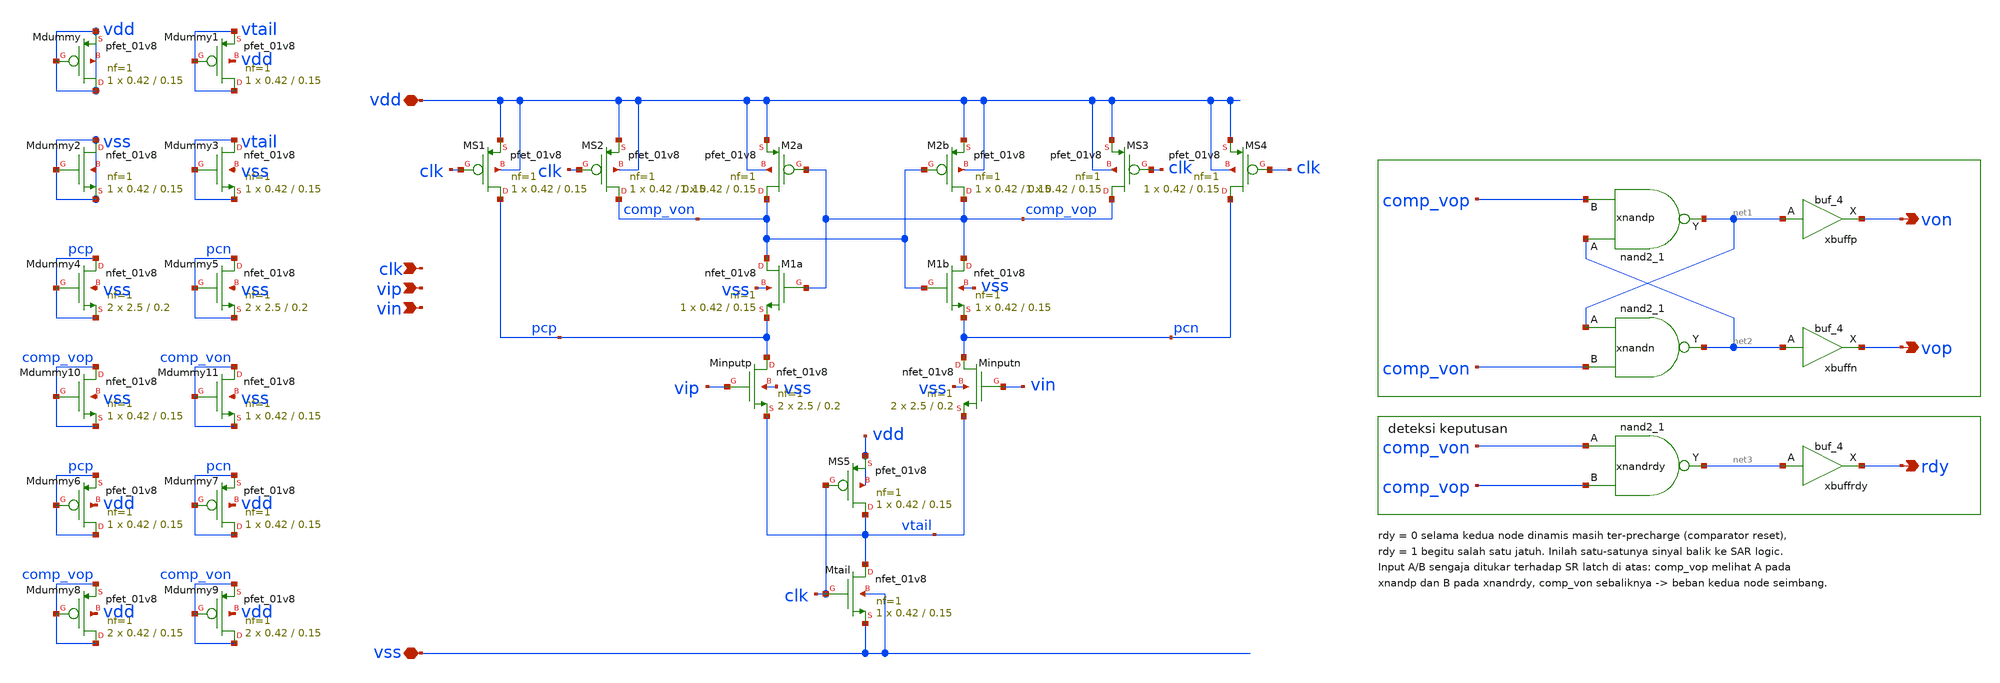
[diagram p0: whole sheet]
** sch_path: xschem/sar-adc/comparator.sch
**.subckt comparator clk vip vin vdd vss vop von rdy
*.ipin clk
*.ipin vip
*.ipin vin
*.iopin vdd
*.iopin vss
*.opin vop
*.opin von
*.opin rdy
XMinputp pcp vip vtail vss sky130_fd_pr__nfet_01v8 L=0.2 W=2.5 nf=1 ad='int((1 + 1)/2) * 2.5 / 1 * 0.29'
+ as='int((1 + 2)/2) * 2.5 / 1 * 0.29' pd='2*int((1 + 1)/2) * (2.5 / 1 + 0.29)' ps='2*int((1 + 2)/2) * (2.5 / 1 + 0.29)'
+ nrd='0.29 / 2.5 ' nrs='0.29 / 2.5 ' sa=0 sb=0 sd=0 mult=2 m=2
XMinputn pcn vin vtail vss sky130_fd_pr__nfet_01v8 L=0.2 W=2.5 nf=1 ad='int((1 + 1)/2) * 2.5 / 1 * 0.29'
+ as='int((1 + 2)/2) * 2.5 / 1 * 0.29' pd='2*int((1 + 1)/2) * (2.5 / 1 + 0.29)' ps='2*int((1 + 2)/2) * (2.5 / 1 + 0.29)'
+ nrd='0.29 / 2.5 ' nrs='0.29 / 2.5 ' sa=0 sb=0 sd=0 mult=2 m=2
XM1a comp_von comp_vop pcp vss sky130_fd_pr__nfet_01v8 L=0.15 W=0.42 nf=1 ad='int((1 + 1)/2) * 0.42 / 1 * 0.29'
+ as='int((1 + 2)/2) * 0.42 / 1 * 0.29' pd='2*int((1 + 1)/2) * (0.42 / 1 + 0.29)' ps='2*int((1 + 2)/2) * (0.42 / 1 + 0.29)'
+ nrd='0.29 / 0.42 ' nrs='0.29 / 0.42 ' sa=0 sb=0 sd=0 mult=1 m=1
XM1b comp_vop comp_von pcn vss sky130_fd_pr__nfet_01v8 L=0.15 W=0.42 nf=1 ad='int((1 + 1)/2) * 0.42 / 1 * 0.29'
+ as='int((1 + 2)/2) * 0.42 / 1 * 0.29' pd='2*int((1 + 1)/2) * (0.42 / 1 + 0.29)' ps='2*int((1 + 2)/2) * (0.42 / 1 + 0.29)'
+ nrd='0.29 / 0.42 ' nrs='0.29 / 0.42 ' sa=0 sb=0 sd=0 mult=1 m=1
XM2a comp_von comp_vop vdd vdd sky130_fd_pr__pfet_01v8 L=0.15 W=0.42 nf=1 ad='int((1 + 1)/2) * 0.42 / 1 * 0.29'
+ as='int((1 + 2)/2) * 0.42 / 1 * 0.29' pd='2*int((1 + 1)/2) * (0.42 / 1 + 0.29)' ps='2*int((1 + 2)/2) * (0.42 / 1 + 0.29)'
+ nrd='0.29 / 0.42 ' nrs='0.29 / 0.42 ' sa=0 sb=0 sd=0 mult=1 m=1
XM2b comp_vop comp_von vdd vdd sky130_fd_pr__pfet_01v8 L=0.15 W=0.42 nf=1 ad='int((1 + 1)/2) * 0.42 / 1 * 0.29'
+ as='int((1 + 2)/2) * 0.42 / 1 * 0.29' pd='2*int((1 + 1)/2) * (0.42 / 1 + 0.29)' ps='2*int((1 + 2)/2) * (0.42 / 1 + 0.29)'
+ nrd='0.29 / 0.42 ' nrs='0.29 / 0.42 ' sa=0 sb=0 sd=0 mult=1 m=1
XMtail vtail clk vss vss sky130_fd_pr__nfet_01v8 L=0.15 W=0.42 nf=1 ad='int((1 + 1)/2) * 0.42 / 1 * 0.29'
+ as='int((1 + 2)/2) * 0.42 / 1 * 0.29' pd='2*int((1 + 1)/2) * (0.42 / 1 + 0.29)' ps='2*int((1 + 2)/2) * (0.42 / 1 + 0.29)'
+ nrd='0.29 / 0.42 ' nrs='0.29 / 0.42 ' sa=0 sb=0 sd=0 mult=1 m=1
XMS3 comp_vop clk vdd vdd sky130_fd_pr__pfet_01v8 L=0.15 W=0.42 nf=1 ad='int((1 + 1)/2) * 0.42 / 1 * 0.29'
+ as='int((1 + 2)/2) * 0.42 / 1 * 0.29' pd='2*int((1 + 1)/2) * (0.42 / 1 + 0.29)' ps='2*int((1 + 2)/2) * (0.42 / 1 + 0.29)'
+ nrd='0.29 / 0.42 ' nrs='0.29 / 0.42 ' sa=0 sb=0 sd=0 mult=1 m=1
XMS2 comp_von clk vdd vdd sky130_fd_pr__pfet_01v8 L=0.15 W=0.42 nf=1 ad='int((1 + 1)/2) * 0.42 / 1 * 0.29'
+ as='int((1 + 2)/2) * 0.42 / 1 * 0.29' pd='2*int((1 + 1)/2) * (0.42 / 1 + 0.29)' ps='2*int((1 + 2)/2) * (0.42 / 1 + 0.29)'
+ nrd='0.29 / 0.42 ' nrs='0.29 / 0.42 ' sa=0 sb=0 sd=0 mult=1 m=1
XMS4 pcn clk vdd vdd sky130_fd_pr__pfet_01v8 L=0.15 W=0.42 nf=1 ad='int((1 + 1)/2) * 0.42 / 1 * 0.29'
+ as='int((1 + 2)/2) * 0.42 / 1 * 0.29' pd='2*int((1 + 1)/2) * (0.42 / 1 + 0.29)' ps='2*int((1 + 2)/2) * (0.42 / 1 + 0.29)'
+ nrd='0.29 / 0.42 ' nrs='0.29 / 0.42 ' sa=0 sb=0 sd=0 mult=1 m=1
XMS1 pcp clk vdd vdd sky130_fd_pr__pfet_01v8 L=0.15 W=0.42 nf=1 ad='int((1 + 1)/2) * 0.42 / 1 * 0.29'
+ as='int((1 + 2)/2) * 0.42 / 1 * 0.29' pd='2*int((1 + 1)/2) * (0.42 / 1 + 0.29)' ps='2*int((1 + 2)/2) * (0.42 / 1 + 0.29)'
+ nrd='0.29 / 0.42 ' nrs='0.29 / 0.42 ' sa=0 sb=0 sd=0 mult=1 m=1
xnandp net2 comp_vop vss vss vdd vdd net1 sky130_fd_sc_hd__nand2_1
xnandn net1 comp_von vss vss vdd vdd net2 sky130_fd_sc_hd__nand2_1
xbuffp net1 vss vss vdd vdd von sky130_fd_sc_hd__buf_4
xbuffn net2 vss vss vdd vdd vop sky130_fd_sc_hd__buf_4
xnandrdy comp_von comp_vop vss vss vdd vdd net3 sky130_fd_sc_hd__nand2_1
xbuffrdy net3 vss vss vdd vdd rdy sky130_fd_sc_hd__buf_4
XMS5 vtail clk vdd vdd sky130_fd_pr__pfet_01v8 L=0.15 W=0.42 nf=1 ad='int((1 + 1)/2) * 0.42 / 1 * 0.29'
+ as='int((1 + 2)/2) * 0.42 / 1 * 0.29' pd='2*int((1 + 1)/2) * (0.42 / 1 + 0.29)' ps='2*int((1 + 2)/2) * (0.42 / 1 + 0.29)'
+ nrd='0.29 / 0.42 ' nrs='0.29 / 0.42 ' sa=0 sb=0 sd=0 mult=1 m=1
XMdummy vdd vdd vdd vdd sky130_fd_pr__pfet_01v8 L=0.15 W=0.42 nf=1 ad='int((1 + 1)/2) * 0.42 / 1 * 0.29'
+ as='int((1 + 2)/2) * 0.42 / 1 * 0.29' pd='2*int((1 + 1)/2) * (0.42 / 1 + 0.29)' ps='2*int((1 + 2)/2) * (0.42 / 1 + 0.29)'
+ nrd='0.29 / 0.42 ' nrs='0.29 / 0.42 ' sa=0 sb=0 sd=0 mult=1 m=1
XMdummy1 vtail vtail vtail vdd sky130_fd_pr__pfet_01v8 L=0.15 W=0.42 nf=1 ad='int((1 + 1)/2) * 0.42 / 1 * 0.29'
+ as='int((1 + 2)/2) * 0.42 / 1 * 0.29' pd='2*int((1 + 1)/2) * (0.42 / 1 + 0.29)' ps='2*int((1 + 2)/2) * (0.42 / 1 + 0.29)'
+ nrd='0.29 / 0.42 ' nrs='0.29 / 0.42 ' sa=0 sb=0 sd=0 mult=1 m=1
XMdummy2 vss vss vss vss sky130_fd_pr__nfet_01v8 L=0.15 W=0.42 nf=1 ad='int((1 + 1)/2) * 0.42 / 1 * 0.29'
+ as='int((1 + 2)/2) * 0.42 / 1 * 0.29' pd='2*int((1 + 1)/2) * (0.42 / 1 + 0.29)' ps='2*int((1 + 2)/2) * (0.42 / 1 + 0.29)'
+ nrd='0.29 / 0.42 ' nrs='0.29 / 0.42 ' sa=0 sb=0 sd=0 mult=1 m=1
XMdummy3 vtail vtail vtail vss sky130_fd_pr__nfet_01v8 L=0.15 W=0.42 nf=1 ad='int((1 + 1)/2) * 0.42 / 1 * 0.29'
+ as='int((1 + 2)/2) * 0.42 / 1 * 0.29' pd='2*int((1 + 1)/2) * (0.42 / 1 + 0.29)' ps='2*int((1 + 2)/2) * (0.42 / 1 + 0.29)'
+ nrd='0.29 / 0.42 ' nrs='0.29 / 0.42 ' sa=0 sb=0 sd=0 mult=1 m=1
XMdummy4 pcp pcp pcp vss sky130_fd_pr__nfet_01v8 L=0.2 W=2.5 nf=1 ad='int((1 + 1)/2) * 2.5 / 1 * 0.29'
+ as='int((1 + 2)/2) * 2.5 / 1 * 0.29' pd='2*int((1 + 1)/2) * (2.5 / 1 + 0.29)' ps='2*int((1 + 2)/2) * (2.5 / 1 + 0.29)'
+ nrd='0.29 / 2.5 ' nrs='0.29 / 2.5 ' sa=0 sb=0 sd=0 mult=2 m=2
XMdummy5 pcn pcn pcn vss sky130_fd_pr__nfet_01v8 L=0.2 W=2.5 nf=1 ad='int((1 + 1)/2) * 2.5 / 1 * 0.29'
+ as='int((1 + 2)/2) * 2.5 / 1 * 0.29' pd='2*int((1 + 1)/2) * (2.5 / 1 + 0.29)' ps='2*int((1 + 2)/2) * (2.5 / 1 + 0.29)'
+ nrd='0.29 / 2.5 ' nrs='0.29 / 2.5 ' sa=0 sb=0 sd=0 mult=2 m=2
XMdummy10 comp_vop comp_vop comp_vop vss sky130_fd_pr__nfet_01v8 L=0.15 W=0.42 nf=1 ad='int((1 + 1)/2) * 0.42 / 1 * 0.29'
+ as='int((1 + 2)/2) * 0.42 / 1 * 0.29' pd='2*int((1 + 1)/2) * (0.42 / 1 + 0.29)' ps='2*int((1 + 2)/2) * (0.42 / 1 + 0.29)'
+ nrd='0.29 / 0.42 ' nrs='0.29 / 0.42 ' sa=0 sb=0 sd=0 mult=1 m=1
XMdummy11 comp_von comp_von comp_von vss sky130_fd_pr__nfet_01v8 L=0.15 W=0.42 nf=1 ad='int((1 + 1)/2) * 0.42 / 1 * 0.29'
+ as='int((1 + 2)/2) * 0.42 / 1 * 0.29' pd='2*int((1 + 1)/2) * (0.42 / 1 + 0.29)' ps='2*int((1 + 2)/2) * (0.42 / 1 + 0.29)'
+ nrd='0.29 / 0.42 ' nrs='0.29 / 0.42 ' sa=0 sb=0 sd=0 mult=1 m=1
XMdummy6 pcp pcp pcp vdd sky130_fd_pr__pfet_01v8 L=0.15 W=0.42 nf=1 ad='int((1 + 1)/2) * 0.42 / 1 * 0.29'
+ as='int((1 + 2)/2) * 0.42 / 1 * 0.29' pd='2*int((1 + 1)/2) * (0.42 / 1 + 0.29)' ps='2*int((1 + 2)/2) * (0.42 / 1 + 0.29)'
+ nrd='0.29 / 0.42 ' nrs='0.29 / 0.42 ' sa=0 sb=0 sd=0 mult=1 m=1
XMdummy7 pcn pcn pcn vdd sky130_fd_pr__pfet_01v8 L=0.15 W=0.42 nf=1 ad='int((1 + 1)/2) * 0.42 / 1 * 0.29'
+ as='int((1 + 2)/2) * 0.42 / 1 * 0.29' pd='2*int((1 + 1)/2) * (0.42 / 1 + 0.29)' ps='2*int((1 + 2)/2) * (0.42 / 1 + 0.29)'
+ nrd='0.29 / 0.42 ' nrs='0.29 / 0.42 ' sa=0 sb=0 sd=0 mult=1 m=1
XMdummy8 comp_vop comp_vop comp_vop vdd sky130_fd_pr__pfet_01v8 L=0.15 W=0.42 nf=1 ad='int((1 + 1)/2) * 0.42 / 1 * 0.29'
+ as='int((1 + 2)/2) * 0.42 / 1 * 0.29' pd='2*int((1 + 1)/2) * (0.42 / 1 + 0.29)' ps='2*int((1 + 2)/2) * (0.42 / 1 + 0.29)'
+ nrd='0.29 / 0.42 ' nrs='0.29 / 0.42 ' sa=0 sb=0 sd=0 mult=2 m=2
XMdummy9 comp_von comp_von comp_von vdd sky130_fd_pr__pfet_01v8 L=0.15 W=0.42 nf=1 ad='int((1 + 1)/2) * 0.42 / 1 * 0.29'
+ as='int((1 + 2)/2) * 0.42 / 1 * 0.29' pd='2*int((1 + 1)/2) * (0.42 / 1 + 0.29)' ps='2*int((1 + 2)/2) * (0.42 / 1 + 0.29)'
+ nrd='0.29 / 0.42 ' nrs='0.29 / 0.42 ' sa=0 sb=0 sd=0 mult=2 m=2
**.ends
.end
